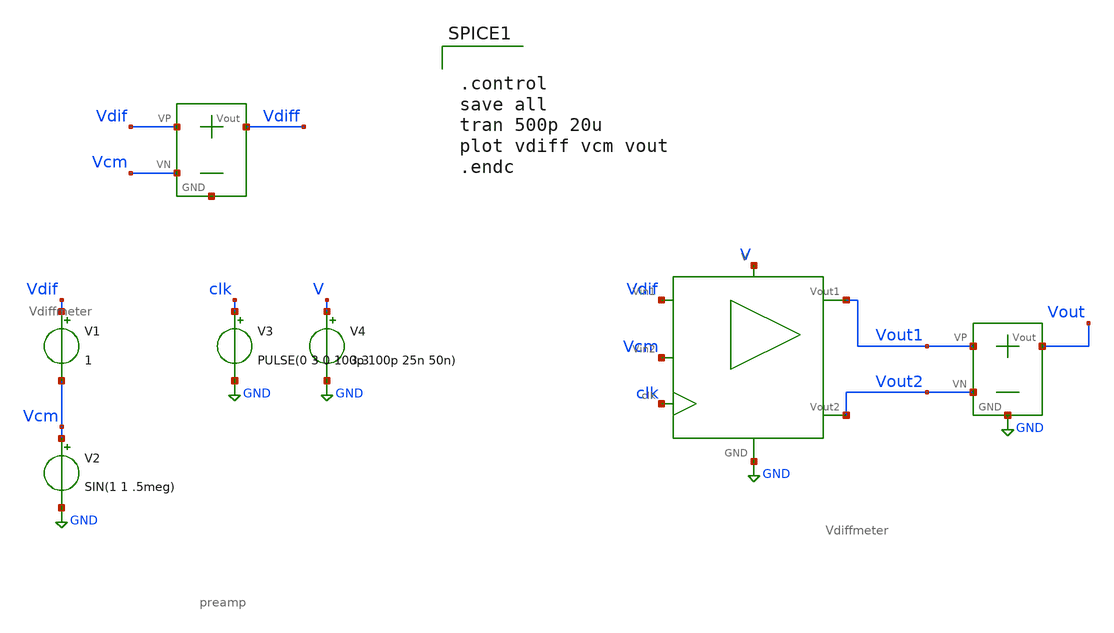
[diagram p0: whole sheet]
** sch_path: SAR_ADC/xschem/test/preamp_tb/vdif_DC-vcm_sin__tb.sch
**.subckt vdif_DC-vcm_sin__tb
V1 Vdif Vcm 1
V2 Vcm GND SIN(1 1 .5meg)
V3 clk GND PULSE(0 3 0 100p 100p 25n 50n)
V4 V GND 3.3
X1 V GND Vdif clk Vout1 Vout2 Vcm preamp
X3 Vout1 Vout2 Vout GND Vdiffmeter
X2 Vdif Vcm Vdiff net1 Vdiffmeter
**** begin user architecture code


.control
save all
tran 500p 20u
plot vdiff vcm vout
.endc


.include /foss/pdks/gf180mcuC/libs.tech/ngspice/design.ngspice
.lib /foss/pdks/gf180mcuC/libs.tech/ngspice/sm141064.ngspice typical

**** end user architecture code
**.ends
.GLOBAL GND
.end
